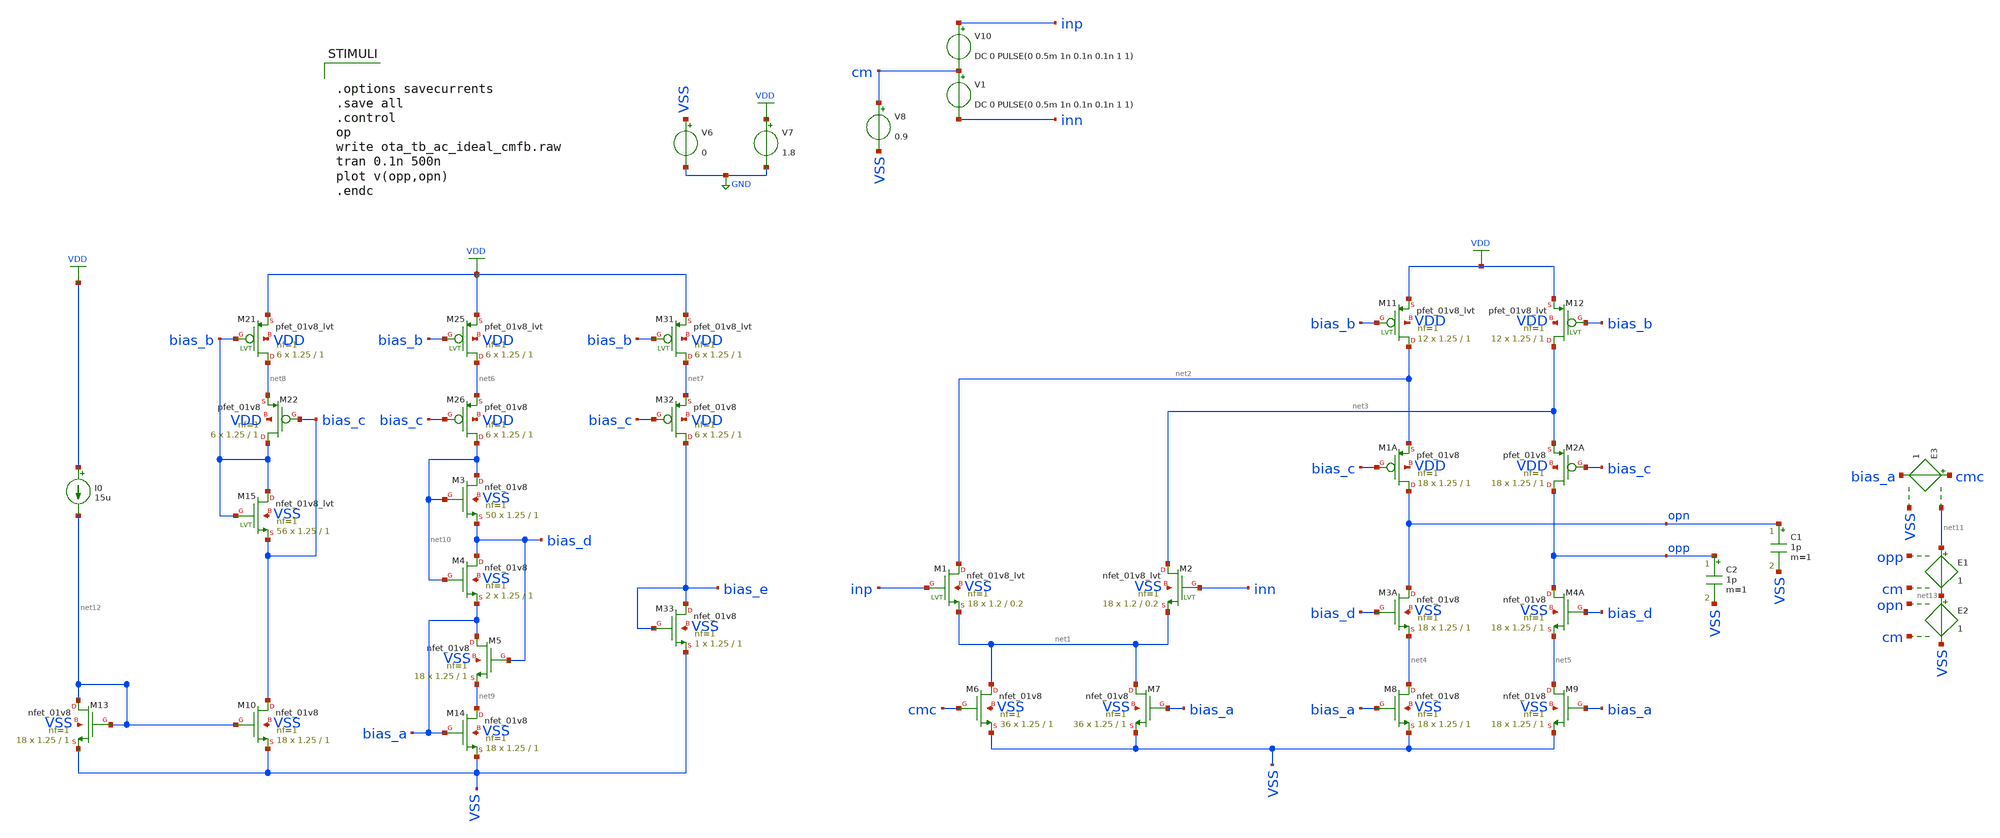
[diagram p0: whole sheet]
** sch_path: verification/schematic/ota_tb_ac_ideal_cmfb.sch
**.subckt ota_tb_ac_ideal_cmfb
XM1 net2 inp net1 VSS sky130_fd_pr__nfet_01v8_lvt L=0.2 W=1.2 nf=1 ad='int((nf+1)/2) * W/nf * 0.29' as='int((nf+2)/2) * W/nf * 0.29'
+ pd='2*int((nf+1)/2) * (W/nf + 0.29)' ps='2*int((nf+2)/2) * (W/nf + 0.29)' nrd='0.29 / W' nrs='0.29 / W'
+ sa=0 sb=0 sd=0 mult=18 m=18
XM2 net3 inn net1 VSS sky130_fd_pr__nfet_01v8_lvt L=0.2 W=1.2 nf=1 ad='int((nf+1)/2) * W/nf * 0.29' as='int((nf+2)/2) * W/nf * 0.29'
+ pd='2*int((nf+1)/2) * (W/nf + 0.29)' ps='2*int((nf+2)/2) * (W/nf + 0.29)' nrd='0.29 / W' nrs='0.29 / W'
+ sa=0 sb=0 sd=0 mult=18 m=18
XM6 net1 cmc VSS VSS sky130_fd_pr__nfet_01v8 L=1 W=1.25 nf=1 ad='int((nf+1)/2) * W/nf * 0.29' as='int((nf+2)/2) * W/nf * 0.29'
+ pd='2*int((nf+1)/2) * (W/nf + 0.29)' ps='2*int((nf+2)/2) * (W/nf + 0.29)' nrd='0.29 / W' nrs='0.29 / W'
+ sa=0 sb=0 sd=0 mult=36 m=36
XM7 net1 bias_a VSS VSS sky130_fd_pr__nfet_01v8 L=1 W=1.25 nf=1 ad='int((nf+1)/2) * W/nf * 0.29' as='int((nf+2)/2) * W/nf * 0.29'
+ pd='2*int((nf+1)/2) * (W/nf + 0.29)' ps='2*int((nf+2)/2) * (W/nf + 0.29)' nrd='0.29 / W' nrs='0.29 / W'
+ sa=0 sb=0 sd=0 mult=36 m=36
XM11 net2 bias_b VDD VDD sky130_fd_pr__pfet_01v8_lvt L=1 W=1.25 nf=1 ad='int((nf+1)/2) * W/nf * 0.29'
+ as='int((nf+2)/2) * W/nf * 0.29' pd='2*int((nf+1)/2) * (W/nf + 0.29)' ps='2*int((nf+2)/2) * (W/nf + 0.29)'
+ nrd='0.29 / W' nrs='0.29 / W' sa=0 sb=0 sd=0 mult=12 m=12
XM12 net3 bias_b VDD VDD sky130_fd_pr__pfet_01v8_lvt L=1 W=1.25 nf=1 ad='int((nf+1)/2) * W/nf * 0.29'
+ as='int((nf+2)/2) * W/nf * 0.29' pd='2*int((nf+1)/2) * (W/nf + 0.29)' ps='2*int((nf+2)/2) * (W/nf + 0.29)'
+ nrd='0.29 / W' nrs='0.29 / W' sa=0 sb=0 sd=0 mult=12 m=12
XM1A opn bias_c net2 VDD sky130_fd_pr__pfet_01v8 L=1 W=1.25 nf=1 ad='int((nf+1)/2) * W/nf * 0.29' as='int((nf+2)/2) * W/nf * 0.29'
+ pd='2*int((nf+1)/2) * (W/nf + 0.29)' ps='2*int((nf+2)/2) * (W/nf + 0.29)' nrd='0.29 / W' nrs='0.29 / W'
+ sa=0 sb=0 sd=0 mult=18 m=18
XM2A opp bias_c net3 VDD sky130_fd_pr__pfet_01v8 L=1 W=1.25 nf=1 ad='int((nf+1)/2) * W/nf * 0.29' as='int((nf+2)/2) * W/nf * 0.29'
+ pd='2*int((nf+1)/2) * (W/nf + 0.29)' ps='2*int((nf+2)/2) * (W/nf + 0.29)' nrd='0.29 / W' nrs='0.29 / W'
+ sa=0 sb=0 sd=0 mult=18 m=18
XM3A opn bias_d net4 VSS sky130_fd_pr__nfet_01v8 L=1 W=1.25 nf=1 ad='int((nf+1)/2) * W/nf * 0.29' as='int((nf+2)/2) * W/nf * 0.29'
+ pd='2*int((nf+1)/2) * (W/nf + 0.29)' ps='2*int((nf+2)/2) * (W/nf + 0.29)' nrd='0.29 / W' nrs='0.29 / W'
+ sa=0 sb=0 sd=0 mult=18 m=18
XM4A opp bias_d net5 VSS sky130_fd_pr__nfet_01v8 L=1 W=1.25 nf=1 ad='int((nf+1)/2) * W/nf * 0.29' as='int((nf+2)/2) * W/nf * 0.29'
+ pd='2*int((nf+1)/2) * (W/nf + 0.29)' ps='2*int((nf+2)/2) * (W/nf + 0.29)' nrd='0.29 / W' nrs='0.29 / W'
+ sa=0 sb=0 sd=0 mult=18 m=18
XM8 net4 bias_a VSS VSS sky130_fd_pr__nfet_01v8 L=1 W=1.25 nf=1 ad='int((nf+1)/2) * W/nf * 0.29' as='int((nf+2)/2) * W/nf * 0.29'
+ pd='2*int((nf+1)/2) * (W/nf + 0.29)' ps='2*int((nf+2)/2) * (W/nf + 0.29)' nrd='0.29 / W' nrs='0.29 / W'
+ sa=0 sb=0 sd=0 mult=18 m=18
XM9 net5 bias_a VSS VSS sky130_fd_pr__nfet_01v8 L=1 W=1.25 nf=1 ad='int((nf+1)/2) * W/nf * 0.29' as='int((nf+2)/2) * W/nf * 0.29'
+ pd='2*int((nf+1)/2) * (W/nf + 0.29)' ps='2*int((nf+2)/2) * (W/nf + 0.29)' nrd='0.29 / W' nrs='0.29 / W'
+ sa=0 sb=0 sd=0 mult=18 m=18
V6 VSS GND 0
V7 VDD GND 1.8
V8 cm VSS 0.9
V10 inp cm DC 0 PULSE(0 0.5m 1n 0.1n 0.1n 1 1)
V1 cm inn DC 0 PULSE(0 0.5m 1n 0.1n 0.1n 1 1)
XM22 bias_b bias_c net8 VDD sky130_fd_pr__pfet_01v8 L=1 W=1.25 nf=1 ad='int((nf+1)/2) * W/nf * 0.29'
+ as='int((nf+2)/2) * W/nf * 0.29' pd='2*int((nf+1)/2) * (W/nf + 0.29)' ps='2*int((nf+2)/2) * (W/nf + 0.29)'
+ nrd='0.29 / W' nrs='0.29 / W' sa=0 sb=0 sd=0 mult=6 m=6
XM26 net10 bias_c net6 VDD sky130_fd_pr__pfet_01v8 L=1 W=1.25 nf=1 ad='int((nf+1)/2) * W/nf * 0.29' as='int((nf+2)/2) * W/nf * 0.29'
+ pd='2*int((nf+1)/2) * (W/nf + 0.29)' ps='2*int((nf+2)/2) * (W/nf + 0.29)' nrd='0.29 / W' nrs='0.29 / W'
+ sa=0 sb=0 sd=0 mult=6 m=6
XM32 bias_e bias_c net7 VDD sky130_fd_pr__pfet_01v8 L=1 W=1.25 nf=1 ad='int((nf+1)/2) * W/nf * 0.29'
+ as='int((nf+2)/2) * W/nf * 0.29' pd='2*int((nf+1)/2) * (W/nf + 0.29)' ps='2*int((nf+2)/2) * (W/nf + 0.29)'
+ nrd='0.29 / W' nrs='0.29 / W' sa=0 sb=0 sd=0 mult=6 m=6
XM33 bias_e bias_e VSS VSS sky130_fd_pr__nfet_01v8 L=1 W=1.25 nf=1 ad='int((nf+1)/2) * W/nf * 0.29' as='int((nf+2)/2) * W/nf * 0.29'
+ pd='2*int((nf+1)/2) * (W/nf + 0.29)' ps='2*int((nf+2)/2) * (W/nf + 0.29)' nrd='0.29 / W' nrs='0.29 / W'
+ sa=0 sb=0 sd=0 mult=1 m=1
XM21 net8 bias_b VDD VDD sky130_fd_pr__pfet_01v8_lvt L=1 W=1.25 nf=1 ad='int((nf+1)/2) * W/nf * 0.29'
+ as='int((nf+2)/2) * W/nf * 0.29' pd='2*int((nf+1)/2) * (W/nf + 0.29)' ps='2*int((nf+2)/2) * (W/nf + 0.29)'
+ nrd='0.29 / W' nrs='0.29 / W' sa=0 sb=0 sd=0 mult=6 m=6
XM25 net6 bias_b VDD VDD sky130_fd_pr__pfet_01v8_lvt L=1 W=1.25 nf=1 ad='int((nf+1)/2) * W/nf * 0.29'
+ as='int((nf+2)/2) * W/nf * 0.29' pd='2*int((nf+1)/2) * (W/nf + 0.29)' ps='2*int((nf+2)/2) * (W/nf + 0.29)'
+ nrd='0.29 / W' nrs='0.29 / W' sa=0 sb=0 sd=0 mult=6 m=6
XM31 net7 bias_b VDD VDD sky130_fd_pr__pfet_01v8_lvt L=1 W=1.25 nf=1 ad='int((nf+1)/2) * W/nf * 0.29'
+ as='int((nf+2)/2) * W/nf * 0.29' pd='2*int((nf+1)/2) * (W/nf + 0.29)' ps='2*int((nf+2)/2) * (W/nf + 0.29)'
+ nrd='0.29 / W' nrs='0.29 / W' sa=0 sb=0 sd=0 mult=6 m=6
XM3 net10 net10 bias_d VSS sky130_fd_pr__nfet_01v8 L=1 W=1.25 nf=1 ad='int((nf+1)/2) * W/nf * 0.29' as='int((nf+2)/2) * W/nf * 0.29'
+ pd='2*int((nf+1)/2) * (W/nf + 0.29)' ps='2*int((nf+2)/2) * (W/nf + 0.29)' nrd='0.29 / W' nrs='0.29 / W'
+ sa=0 sb=0 sd=0 mult=50 m=50
XM4 bias_d net10 bias_a VSS sky130_fd_pr__nfet_01v8 L=1 W=1.25 nf=1 ad='int((nf+1)/2) * W/nf * 0.29'
+ as='int((nf+2)/2) * W/nf * 0.29' pd='2*int((nf+1)/2) * (W/nf + 0.29)' ps='2*int((nf+2)/2) * (W/nf + 0.29)'
+ nrd='0.29 / W' nrs='0.29 / W' sa=0 sb=0 sd=0 mult=2 m=2
XM5 bias_a bias_d net9 VSS sky130_fd_pr__nfet_01v8 L=1 W=1.25 nf=1 ad='int((nf+1)/2) * W/nf * 0.29' as='int((nf+2)/2) * W/nf * 0.29'
+ pd='2*int((nf+1)/2) * (W/nf + 0.29)' ps='2*int((nf+2)/2) * (W/nf + 0.29)' nrd='0.29 / W' nrs='0.29 / W'
+ sa=0 sb=0 sd=0 mult=18 m=18
XM14 net9 bias_a VSS VSS sky130_fd_pr__nfet_01v8 L=1 W=1.25 nf=1 ad='int((nf+1)/2) * W/nf * 0.29' as='int((nf+2)/2) * W/nf * 0.29'
+ pd='2*int((nf+1)/2) * (W/nf + 0.29)' ps='2*int((nf+2)/2) * (W/nf + 0.29)' nrd='0.29 / W' nrs='0.29 / W'
+ sa=0 sb=0 sd=0 mult=18 m=18
XM15 bias_b bias_b bias_c VSS sky130_fd_pr__nfet_01v8_lvt L=1 W=1.25 nf=1 ad='int((nf+1)/2) * W/nf * 0.29'
+ as='int((nf+2)/2) * W/nf * 0.29' pd='2*int((nf+1)/2) * (W/nf + 0.29)' ps='2*int((nf+2)/2) * (W/nf + 0.29)'
+ nrd='0.29 / W' nrs='0.29 / W' sa=0 sb=0 sd=0 mult=56 m=56
E1 net11 net13 opp cm 1
E2 net13 VSS opn cm 1
E3 cmc bias_a net11 VSS 1
C1 opn VSS 1p m=1
C2 opp VSS 1p m=1
XM10 bias_c net12 VSS VSS sky130_fd_pr__nfet_01v8 L=1 W=1.25 nf=1 ad='int((nf+1)/2) * W/nf * 0.29' as='int((nf+2)/2) * W/nf * 0.29'
+ pd='2*int((nf+1)/2) * (W/nf + 0.29)' ps='2*int((nf+2)/2) * (W/nf + 0.29)' nrd='0.29 / W' nrs='0.29 / W'
+ sa=0 sb=0 sd=0 mult=18 m=18
XM13 net12 net12 VSS VSS sky130_fd_pr__nfet_01v8 L=1 W=1.25 nf=1 ad='int((nf+1)/2) * W/nf * 0.29' as='int((nf+2)/2) * W/nf * 0.29'
+ pd='2*int((nf+1)/2) * (W/nf + 0.29)' ps='2*int((nf+2)/2) * (W/nf + 0.29)' nrd='0.29 / W' nrs='0.29 / W'
+ sa=0 sb=0 sd=0 mult=18 m=18
I0 VDD net12 15u
**** begin user architecture code

** opencircuitdesign pdks install
.lib /farmshare/home/classes/ee/372/PDKs/open_pdks_1.0.310/sky130/sky130A/libs.tech/ngspice/sky130.lib.spice tt



.options savecurrents
.save all
.control
op
write ota_tb_ac_ideal_cmfb.raw
tran 0.1n 500n
plot v(opp,opn)
.endc


**** end user architecture code
**.ends
.GLOBAL VDD
.GLOBAL GND
.end
